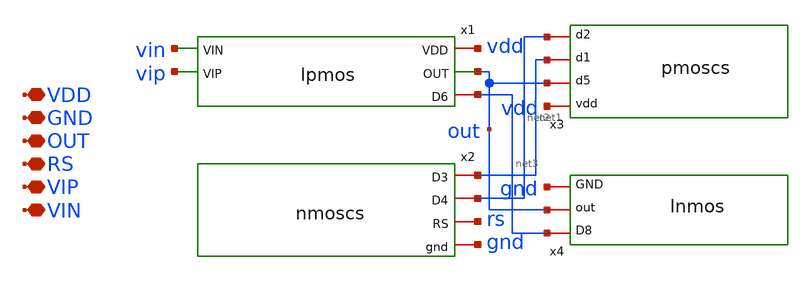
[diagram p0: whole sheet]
** sch_path: mag/opamp.sch
**.subckt opamp VDD GND OUT RS VIP VIN
*.iopin VDD
*.iopin GND
*.iopin OUT
*.iopin RS
*.iopin VIP
*.iopin VIN
x1 vdd vin vip out net3 lpmos
x2 net1 net2 rs gnd nmoscs
x3 vdd out net1 net2 pmoscs
x4 net3 out gnd lnmos
**.ends
.end
